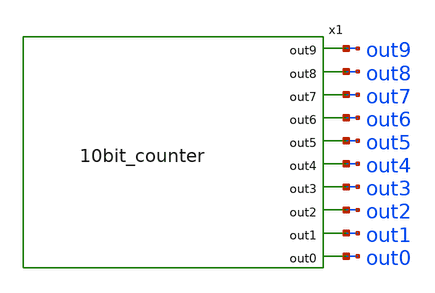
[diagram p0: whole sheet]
** sch_path: DAC/xschem/tb/tb_10bit_counter.sch
**.subckt tb_10bit_counter
x1 out0 out1 out2 out3 out4 out5 out6 out7 out8 out9 10bit_counter
**** begin user architecture code




.control
	tran 1n 25600n
	plot
+ v(out0)+2*v(out1)+4*v(out2)+8*v(out3)+16*v(out4)+32*v(out5)+64*v(out6)+128*v(out7)+256*v(out8)+512*v(out9)
	write tb_10bit_counter.raw
.endc
.save all




**** end user architecture code
**.ends

* expanding   symbol:  10bit_counter.sym # of pins=10
** sym_path: DAC/xschem/10bit_counter.sym
.include /home/junbeom/pico/designs/xschem/10bit_Counter.sp
.end
